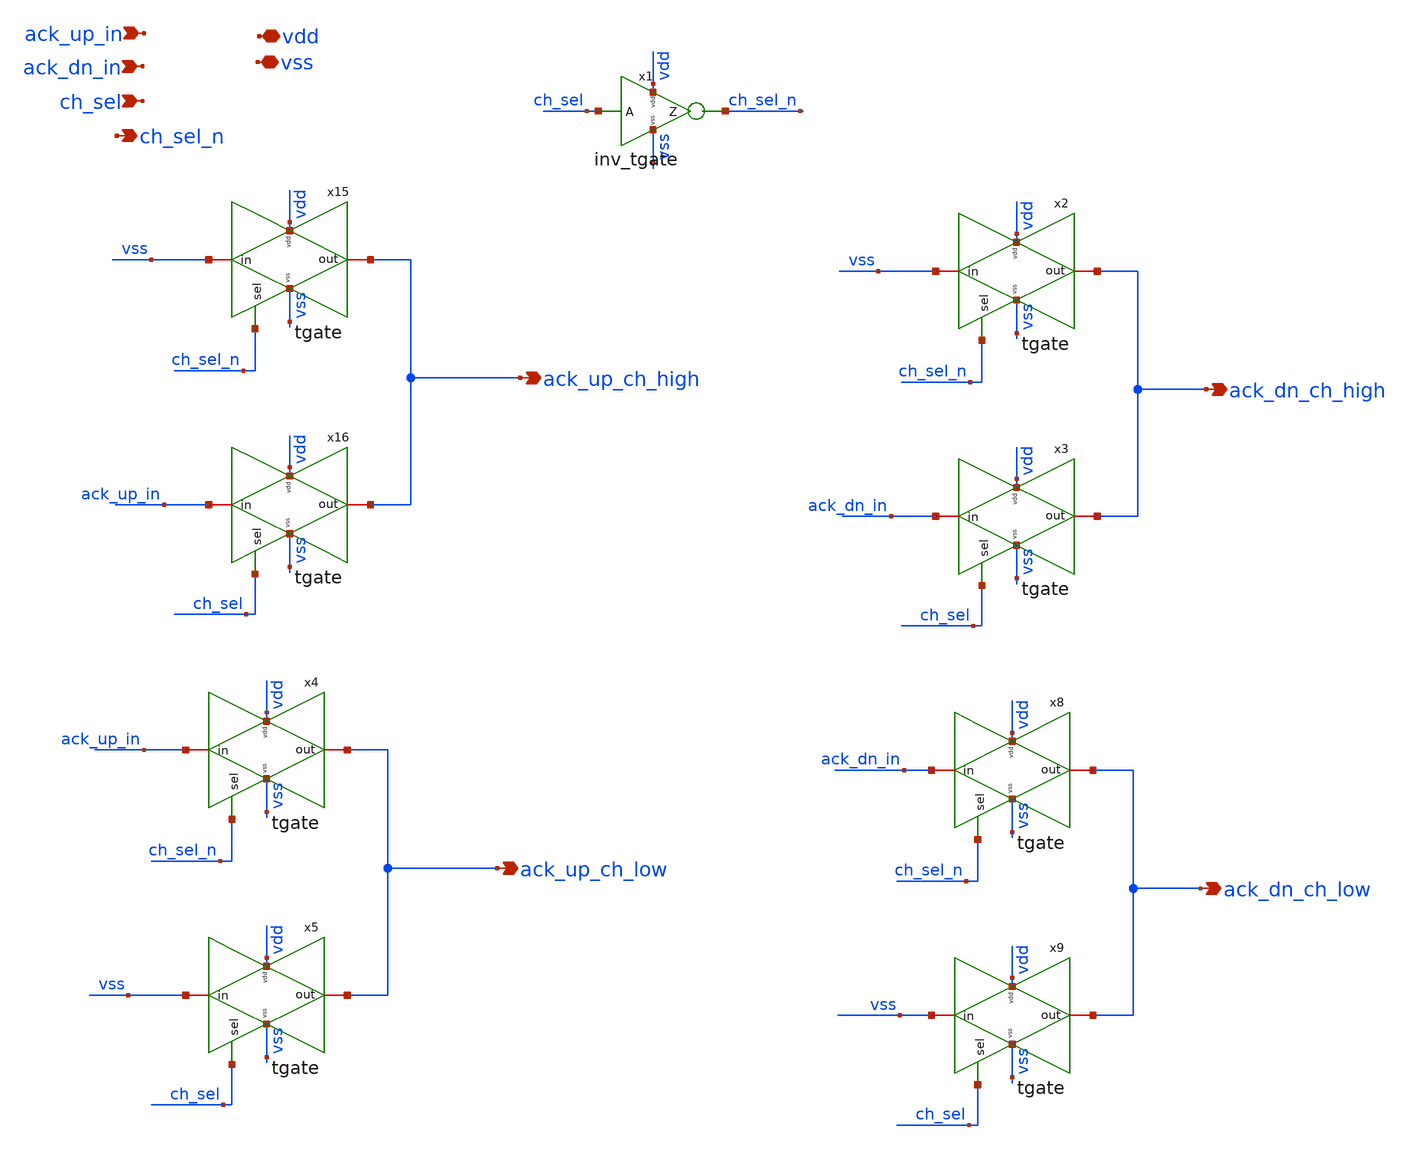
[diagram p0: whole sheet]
** sch_path: v2_feature_extr/ackin_sel.sch
**.subckt ackin_sel ack_up_in ch_sel ack_dn_in vdd vss ack_up_ch_high ack_dn_ch_high ack_up_ch_low
*+ ack_dn_ch_low ch_sel_n
*.ipin ack_up_in
*.ipin ch_sel
*.ipin ack_dn_in
*.iopin vdd
*.iopin vss
*.opin ack_up_ch_high
*.opin ack_dn_ch_high
*.opin ack_up_ch_low
*.opin ack_dn_ch_low
*.opin ch_sel_n
x15 vss vdd vss ack_up_ch_high ch_sel_n tgate
x16 vss vdd ack_up_in ack_up_ch_high ch_sel tgate
x1 vdd ch_sel ch_sel_n vss inv_tgate
x2 vss vdd vss ack_dn_ch_high ch_sel_n tgate
x3 vss vdd ack_dn_in ack_dn_ch_high ch_sel tgate
x8 vss vdd ack_dn_in ack_dn_ch_low ch_sel_n tgate
x9 vss vdd vss ack_dn_ch_low ch_sel tgate
x4 vss vdd ack_up_in ack_up_ch_low ch_sel_n tgate
x5 vss vdd vss ack_up_ch_low ch_sel tgate
**.ends
.end
